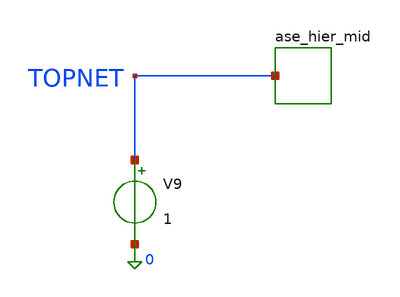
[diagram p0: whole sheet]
** sch_path: tests/headless/fixtures/ase_hier/ase_hier_top.sch
**.subckt ase_hier_top
x1 TOPNET ase_hier_mid
V9 TOPNET 0 1
**.ends

* expanding   symbol:  ase_hier_mid.sym # of pins=1
** sym_path: tests/headless/fixtures/ase_hier/ase_hier_mid.sym
** sch_path: tests/headless/fixtures/ase_hier/ase_hier_mid.sch
.subckt ase_hier_mid A
*.ipin A
x2 A net1 ase_hier_leaf
.ends


* expanding   symbol:  ase_hier_leaf.sym # of pins=2
** sym_path: tests/headless/fixtures/ase_hier/ase_hier_leaf.sym
** sch_path: tests/headless/fixtures/ase_hier/ase_hier_leaf.sch
.subckt ase_hier_leaf A B
*.ipin A
*.opin B
V1 A mid 0
R1 mid 0 1k m=1
.ends

.end
